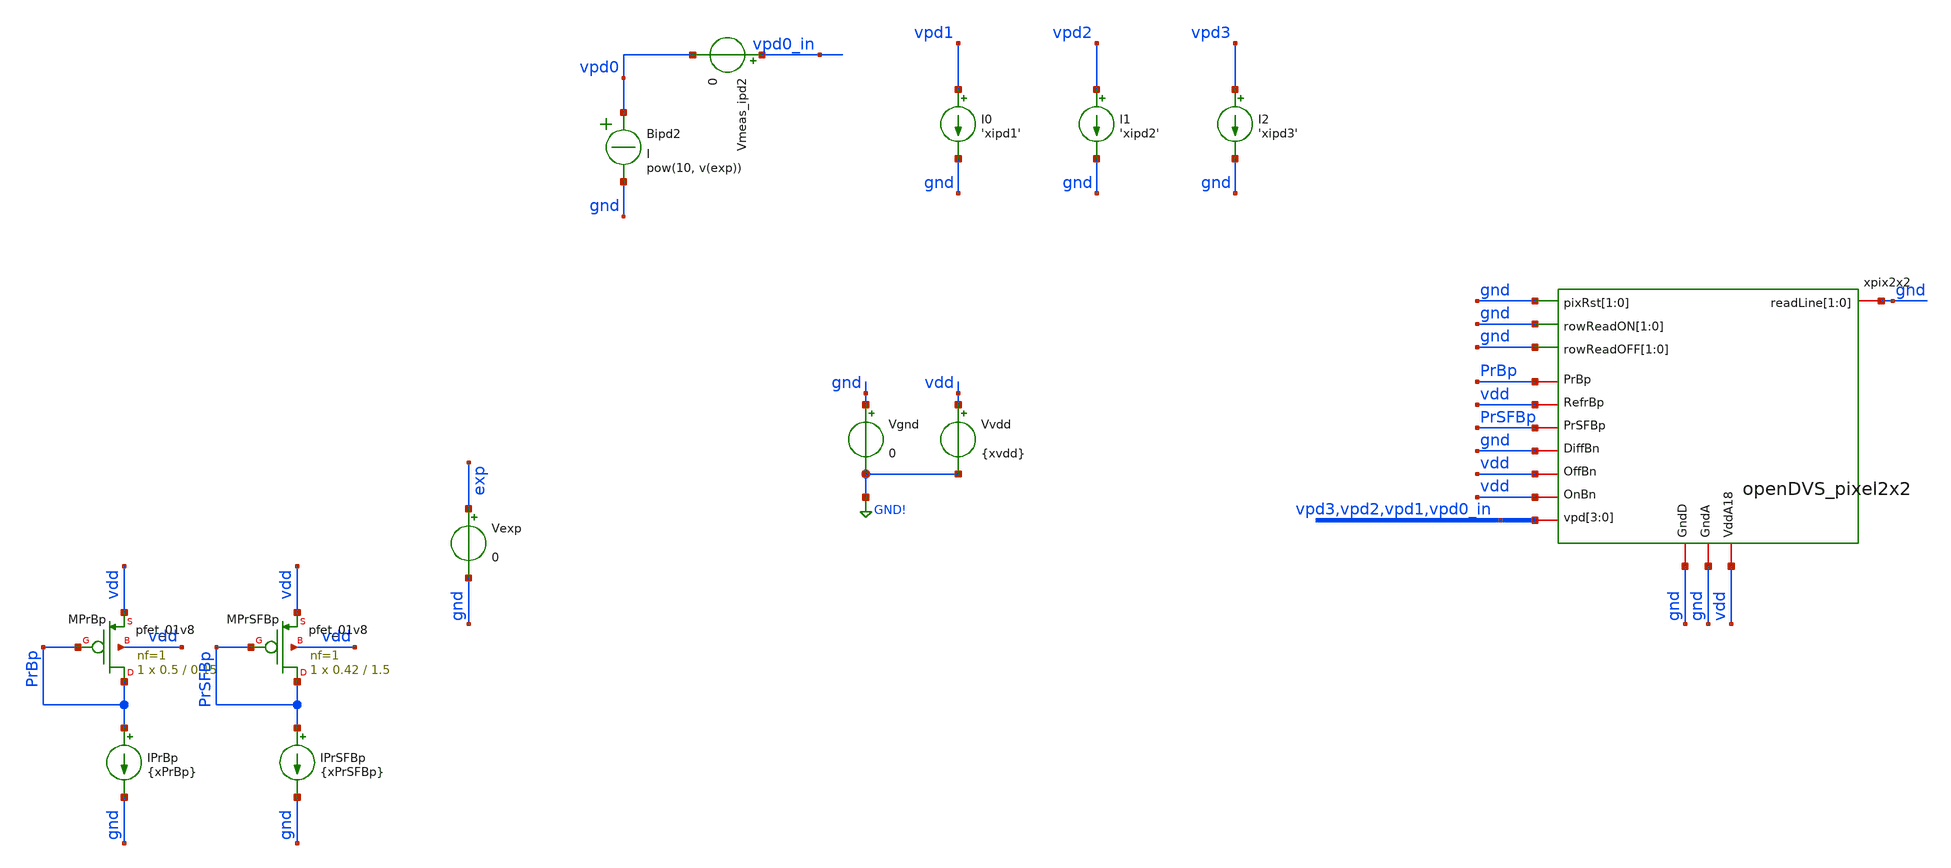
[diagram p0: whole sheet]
** sch_path: analog/xschem/tb_PixelPhotoreceptor_dc_2x2.sch
**.subckt tb_PixelPhotoreceptor_dc_2x2
IPrBp PrBp gnd {xPrBp}
XMPrBp PrBp PrBp vdd vdd sky130_fd_pr__pfet_01v8 L=0.15 W=0.5 nf=1 ad='int((1 + 1)/2) * 0.5 / 1 * 0.29'
+ as='int((1 + 2)/2) * 0.5 / 1 * 0.29' pd='2*int((1 + 1)/2) * (0.5 / 1 + 0.29)' ps='2*int((1 + 2)/2) * (0.5 / 1 + 0.29)'
+ nrd='0.29 / 0.5 ' nrs='0.29 / 0.5 ' sa=0 sb=0 sd=0 mult=1 m=1
IPrSFBp PrSFBp gnd {xPrSFBp}
XMPrSFBp PrSFBp PrSFBp vdd vdd sky130_fd_pr__pfet_01v8 L=1.5 W=0.42 nf=1 ad='int((1 + 1)/2) * 0.42 / 1 * 0.29'
+ as='int((1 + 2)/2) * 0.42 / 1 * 0.29' pd='2*int((1 + 1)/2) * (0.42 / 1 + 0.29)' ps='2*int((1 + 2)/2) * (0.42 / 1 + 0.29)'
+ nrd='0.29 / 0.42 ' nrs='0.29 / 0.42 ' sa=0 sb=0 sd=0 mult=1 m=1
Vexp exp gnd 0
Vgnd gnd GND! 0
Vvdd vdd GND! {xvdd}
xpix2x2 gnd gnd gnd gnd gnd gnd gnd gnd vpd3 vpd2 vpd1 vpd0_in vdd gnd gnd vdd vdd gnd PrSFBp vdd
+ PrBp openDVS_pixel2x2
Bipd2 vpd0 gnd I = pow(10, v(exp))
Vmeas_ipd2 vpd0_in vpd0 0
I0 vpd1 gnd 'xipd1'
I1 vpd2 gnd 'xipd2'
I2 vpd3 gnd 'xipd3'
**** begin user architecture code

** opencircuitdesign pdks install
.lib $::SKYWATER_MODELS/sky130.lib.spice tt



.include /home/rpgraca/research/projects/telluride/2025/nic_eventcam/nic2025_openDVS/analog/xschem/dvs_readout_ctrl.spice

** Set USE_PEX=1 to use extracted netlist instead of schematic
*.include /home/rpgraca/research/projects/telluride/2025/nic_eventcam/nic2025_openDVS/analog/xschem/openDVS_pixel2x2_pex_simple.spice
*.include /home/rpgraca/research/projects/telluride/2025/nic_eventcam/nic2025_openDVS/analog/xschem/openDVS_pixel2x2_pex_r.spice
*.include /home/rpgraca/research/projects/telluride/2025/nic_eventcam/nic2025_openDVS/analog/xschem/openDVS_pixel2x2_pex_cc.spice
*.include /home/rpgraca/research/projects/telluride/2025/nic_eventcam/nic2025_openDVS/analog/xschem/openDVS_pixel2x2_pex_c.spice
.include /home/rpgraca/research/projects/telluride/2025/nic_eventcam/nic2025_openDVS/analog/xschem/openDVS_pixel2x2_pex_rcc.spice
*.include /home/rpgraca/research/projects/telluride/2025/nic_eventcam/nic2025_openDVS/analog/xschem/openDVS_pixel2x2_pex_rc.spice


** Convergence options for nA-range weak-inversion pixel circuit
** gmin=1e-15: at 1V node this is 1fA shunt, negligible vs nA signals
** method=gear: damps numerical ringing on stiff circuits (fast digital + slow analog)
** trtol=1: conservative timestep control prevents overshoot at edges
.option gmin=1e-17 abstol=1e-15 vntol=1e-9 reltol=1e-4 chgtol=1e-16
.option method=gear maxord=2 trtol=1
.option itl1=500 itl2=200 itl4=50
.option gminsteps=200 srcsteps=200
.option ramptime=100n

.dc Vexp -14 -7 0.2


.param xvdd = 1.8
*.param xipd = 1e-9
.param xPrBp = 10n
.param xPrSFBp = 100p
.param xCloadPD = 30f

.param xipd1 = 1n
.param xipd2 = 1n
.param xipd3 = 1n

** xipd swept via Vexp: Iipd uses behavioral expression

*Small Iphoto testing

.save all



**** end user architecture code
**.ends
.GLOBAL GND!
.end
